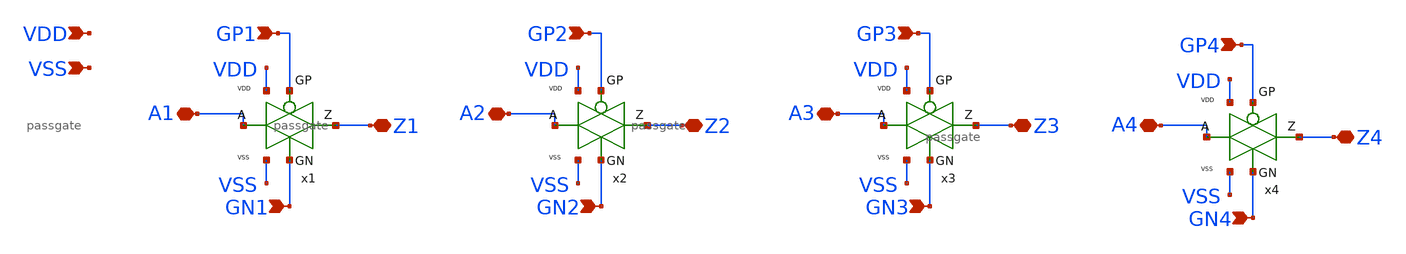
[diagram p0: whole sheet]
** sch_path: xschem/passgatex4.sch
**.subckt passgatex4 VDD VSS GP1 GN1 A1 Z1 GP2 GN2 A2 Z2 GP3 GN3 A3 Z3 GP4 GN4 A4 Z4
*.ipin VDD
*.ipin VSS
*.ipin GP1
*.ipin GN1
*.iopin A1
*.iopin Z1
*.ipin GP2
*.ipin GN2
*.iopin A2
*.iopin Z2
*.ipin GP3
*.ipin GN3
*.iopin A3
*.iopin Z3
*.ipin GP4
*.ipin GN4
*.iopin A4
*.iopin Z4
x1 A1 GN1 GP1 Z1 VDD VSS passgate
x2 A2 GN2 GP2 Z2 VDD VSS passgate
x3 A3 GN3 GP3 Z3 VDD VSS passgate
x4 A4 GN4 GP4 Z4 VDD VSS passgate
**.ends

* expanding   symbol:  passgate.sym # of pins=6
** sym_path: xschem/passgate.sym
** sch_path: xschem/passgate.sch
.subckt passgate A GN GP Z VDD VSS
*.ipin GN
*.ipin VDD
*.ipin VSS
*.ipin GP
*.iopin A
*.iopin Z
XM1 Z GN A VSS sky130_fd_pr__nfet_01v8_lvt L=0.35 W=8 nf=1 ad='int((nf+1)/2) * W/nf * 0.29' as='int((nf+2)/2) * W/nf * 0.29'
+ pd='2*int((nf+1)/2) * (W/nf + 0.29)' ps='2*int((nf+2)/2) * (W/nf + 0.29)' nrd='0.29 / W' nrs='0.29 / W'
+ sa=0 sb=0 sd=0 mult=2 m=2
XM3 Z GP A VDD sky130_fd_pr__pfet_01v8_lvt L=0.35 W=10 nf=1 ad='int((nf+1)/2) * W/nf * 0.29' as='int((nf+2)/2) * W/nf * 0.29'
+ pd='2*int((nf+1)/2) * (W/nf + 0.29)' ps='2*int((nf+2)/2) * (W/nf + 0.29)' nrd='0.29 / W' nrs='0.29 / W'
+ sa=0 sb=0 sd=0 mult=2 m=2
.ends

.end
